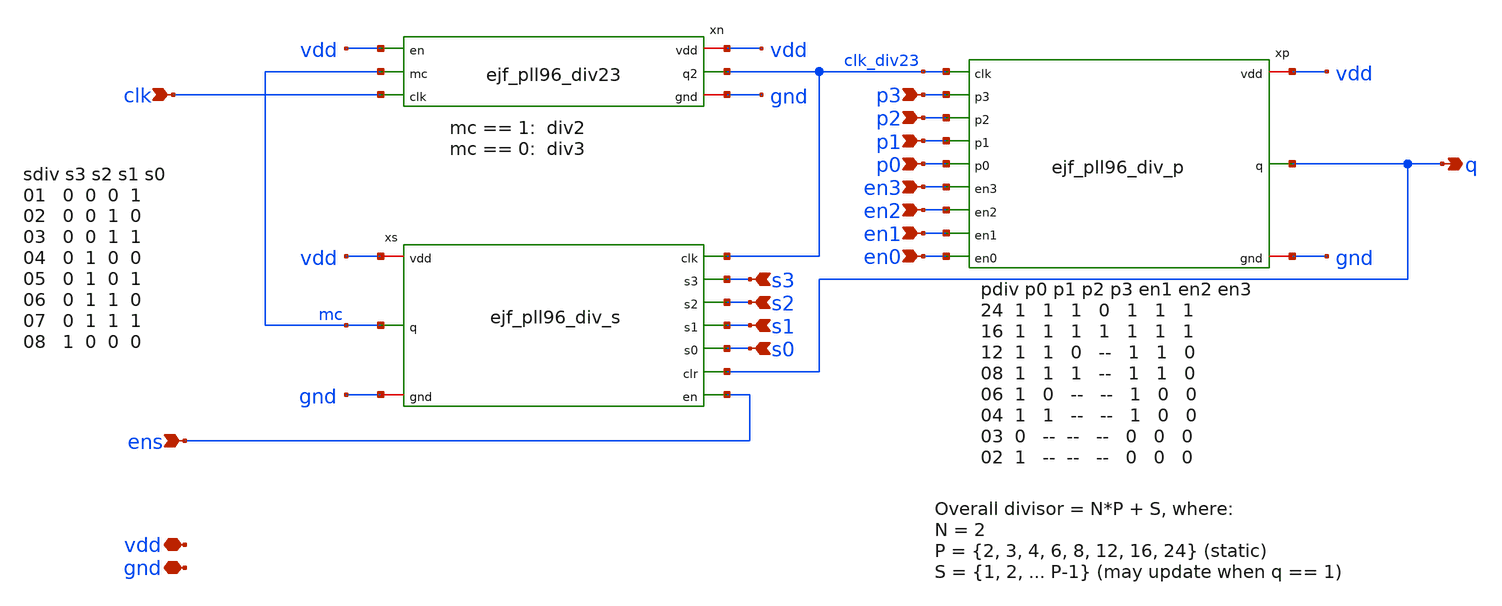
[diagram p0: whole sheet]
** sch_path: xschem/ejf_pll96_div_mm.sch
**.subckt ejf_pll96_div_mm gnd clk q vdd p3 p2 p1 p0 en3 en2 en1 s0 s1 s2 s3 ens en0
*.iopin gnd
*.ipin clk
*.opin q
*.iopin vdd
*.ipin p3
*.ipin p2
*.ipin p1
*.ipin p0
*.ipin en3
*.ipin en2
*.ipin en1
*.ipin s0
*.ipin s1
*.ipin s2
*.ipin s3
*.ipin ens
*.ipin en0
xn clk_div23 clk mc vdd gnd vdd ejf_pll96_div23
xp clk_div23 p0 en1 p1 q en2 p2 en3 p3 vdd gnd en0 ejf_pll96_div_p
xs clk_div23 s0 s1 s3 s2 q mc vdd gnd ens ejf_pll96_div_s
**.ends

* expanding   symbol:  ejf_pll96_div23.sym # of pins=6
** sym_path: xschem/ejf_pll96_div23.sym
** sch_path: xschem/ejf_pll96_div23.sch
.subckt ejf_pll96_div23 q2 clk mc vdd gnd en
*.ipin clk
*.ipin mc
*.opin q2
*.iopin vdd
*.iopin gnd
*.ipin en
x3 q1 mc net1 gnd gnd vdd vdd d2 sky130_fd_sc_ls__o21a_1
x1 clk net1 en gnd gnd vdd vdd q1 sky130_fd_sc_ls__dfstp_2
x2 clk d2 en gnd gnd vdd vdd q2 net1 sky130_fd_sc_ls__dfsbp_2
.ends


* expanding   symbol:  ejf_pll96_div_p.sym # of pins=12
** sym_path: xschem/ejf_pll96_div_p.sym
** sch_path: xschem/ejf_pll96_div_p.sch
.subckt ejf_pll96_div_p clk p0 en1 p1 q en2 p2 en3 p3 vdd gnd en0
*.iopin vdd
*.iopin gnd
*.ipin clk
*.ipin p1
*.ipin p2
*.ipin p3
*.ipin en3
*.ipin en2
*.opin q
*.ipin en1
*.ipin en0
*.ipin p0
x0 q0 clk p0 vdd gnd en0 ejf_pll96_div23
x1 q1 q0 p1 vdd gnd en1 ejf_pll96_div23
x2 q2 q1 p2 vdd gnd en2 ejf_pll96_div23
x3 q3 q2 p3 vdd gnd en3 ejf_pll96_div23
x6 q0 q1 q2 q3 gnd gnd vdd vdd eq0123 sky130_fd_sc_ls__and4_2
x4 clk eq0123 en0 gnd gnd vdd vdd q sky130_fd_sc_ls__dfrtp_2
.ends


* expanding   symbol:  ejf_pll96_div_s.sym # of pins=10
** sym_path: xschem/ejf_pll96_div_s.sym
** sch_path: xschem/ejf_pll96_div_s.sch
.subckt ejf_pll96_div_s clk s0 s1 s3 s2 clr q vdd gnd en
*.ipin s0
*.ipin s1
*.ipin s2
*.ipin s3
*.ipin clk
*.iopin vdd
*.iopin gnd
*.ipin en
*.ipin clr
*.opin q
x1 q0 s0 gnd gnd vdd vdd eq0 sky130_fd_sc_ls__xnor2_1
xdff0 clk q0_b q_b gnd gnd vdd vdd q0 q0_b sky130_fd_sc_ls__dfrbp_1
x5 q1 s1 gnd gnd vdd vdd eq1 sky130_fd_sc_ls__xnor2_1
xdff1 q0_b q1_b q_b gnd gnd vdd vdd q1 q1_b sky130_fd_sc_ls__dfrbp_1
x7 q2 s2 gnd gnd vdd vdd eq2 sky130_fd_sc_ls__xnor2_1
xdff2 q1_b q2_b q_b gnd gnd vdd vdd q2 q2_b sky130_fd_sc_ls__dfrbp_1
x9 q3 s3 gnd gnd vdd vdd eq3 sky130_fd_sc_ls__xnor2_1
xdff3 q2_b q3_b q_b gnd gnd vdd vdd q3 q3_b sky130_fd_sc_ls__dfrbp_1
x8 en gnd gnd vdd vdd en_b sky130_fd_sc_ls__inv_1
x4 q eq0123 en_b gnd gnd vdd vdd q_b sky130_fd_sc_ls__nor3_2
x2 eq3 eq2 eq1 eq0 gnd gnd vdd vdd eq0123 sky130_fd_sc_ls__and4_2
x11 en clr q_b gnd gnd vdd vdd q sky130_fd_sc_ls__a21oi_2
.ends

.end
